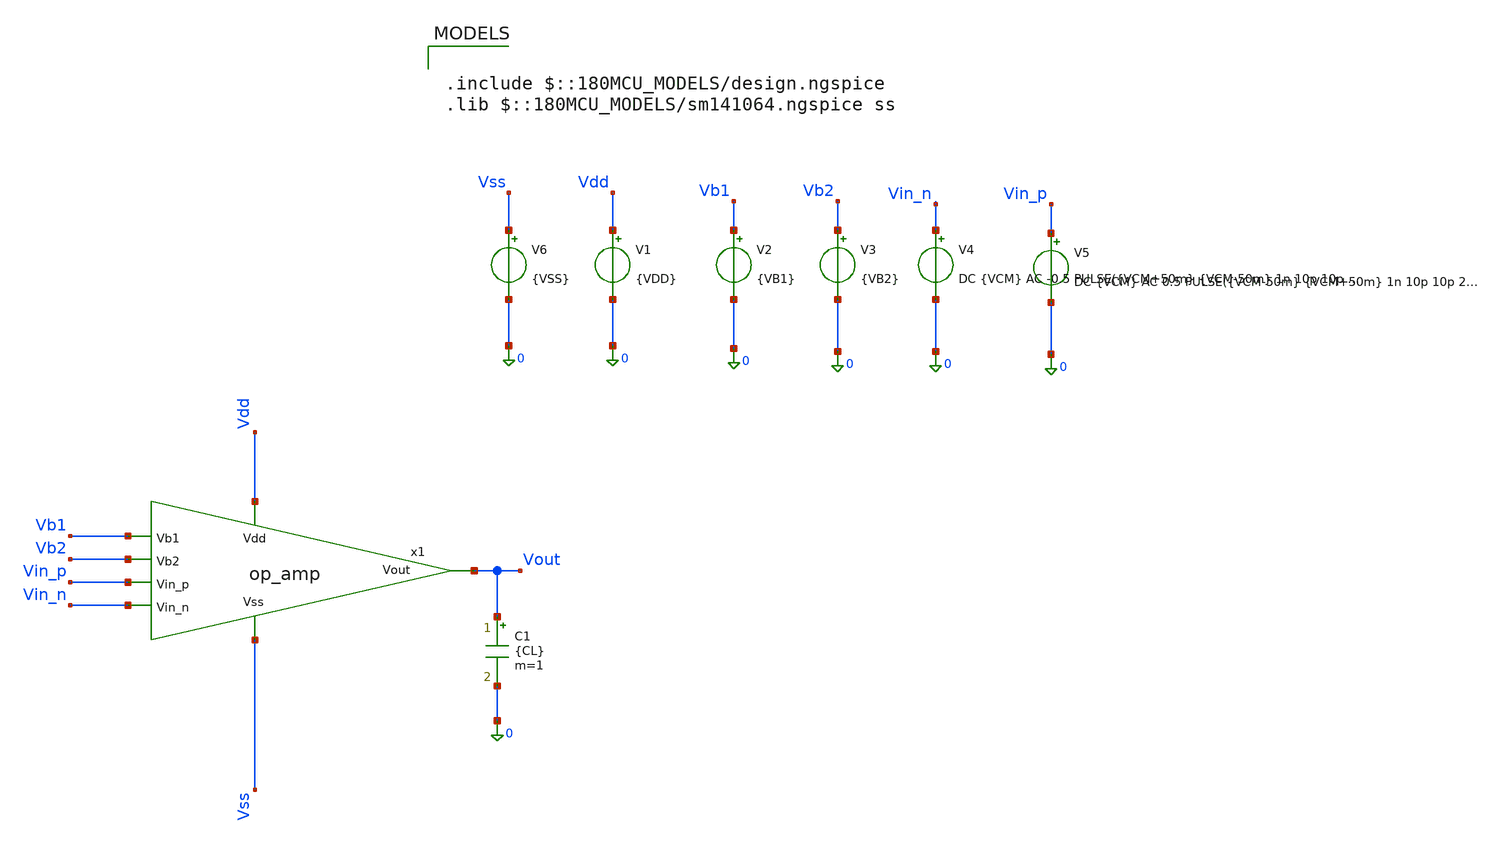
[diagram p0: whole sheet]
** sch_path: blocks/adc/lvds/ota_performance_test.sch
**.subckt ota_performance_test
x1 Vdd Vb1 Vout Vb2 Vin_p Vin_n Vss op_amp
V1 Vdd 0 {VDD}
V2 Vb1 0 {VB1}
V3 Vb2 0 {VB2}
V4 Vin_n 0 DC {VCM} AC -0.5 PULSE({VCM+50m} {VCM-50m} 1n 10p 10p 20n 50n)
V5 Vin_p 0 DC {VCM} AC 0.5 PULSE({VCM-50m} {VCM+50m} 1n 10p 10p 20n 50n)
V6 Vss 0 {VSS}
C1 Vout 0 {CL} m=1
**** begin user architecture code


.param VDD=3.3
.param VSS=0
.param VCM=1.2
.param VB1=0.0
.param VB2=1.65
.param CL=10f
.options temp=27

.control
save all
set filetype=ascii
set wr_singlescale
set wr_vecnames
shell rm /foss/designs/trans_testing/ota_testing/ota_ac.txt
shell rm /foss/designs/trans_testing/ota_testing/ota_tran.txt

op


* AC gain
ac dec 1000 1 500G
let vin_diff_ac = v(Vin_p)-v(Vin_n)
let gain = v(Vout)/vin_diff_ac
wrdata /foss/designs/trans_testing/ota_testing/ota_ac.txt frequency db(gain) real(gain) imag(gain)
plot v(Vout)

* Transient slew rate
tran 1p 100n
let vin_diff = v(Vin_p)-v(Vin_n)
let slew = deriv(v(Vout))
plot v(Vout)

wrdata /foss/designs/trans_testing/ota_testing/ota_tran.txt time v(Vin_p) v(Vin_n) vin_diff v(Vout)
+ slew

.endc



.include $::180MCU_MODELS/design.ngspice
.lib $::180MCU_MODELS/sm141064.ngspice ss

**** end user architecture code
**.ends

* expanding   symbol:  op_amp.sym # of pins=7
** sym_path: blocks/adc/lvds/op_amp.sym
** sch_path: blocks/adc/lvds/op_amp.sch
.subckt op_amp Vdd Vb1 Vout Vb2 Vin_p Vin_n Vss
*.ipin Vdd
*.ipin Vb2
*.ipin Vin_p
*.ipin Vin_n
*.ipin Vb1
*.opin Vout
*.ipin Vss
XM1 net2 net3 Vdd Vdd pfet_03v3 L=0.28u W=10.5u nf=1 ad='int((nf+1)/2) * W/nf * 0.18u' as='int((nf+2)/2) * W/nf * 0.18u'
+ pd='2*int((nf+1)/2) * (W/nf + 0.18u)' ps='2*int((nf+2)/2) * (W/nf + 0.18u)' nrd='0.18u / W' nrs='0.18u / W'
+ sa=0 sb=0 sd=0 m=1
XM2 net1 net4 Vdd Vdd pfet_03v3 L=0.28u W=10.5u nf=1 ad='int((nf+1)/2) * W/nf * 0.18u' as='int((nf+2)/2) * W/nf * 0.18u'
+ pd='2*int((nf+1)/2) * (W/nf + 0.18u)' ps='2*int((nf+2)/2) * (W/nf + 0.18u)' nrd='0.18u / W' nrs='0.18u / W'
+ sa=0 sb=0 sd=0 m=1
XM3 net3 Vb2 net2 Vdd pfet_03v3 L=0.28u W=10.5u nf=1 ad='int((nf+1)/2) * W/nf * 0.18u' as='int((nf+2)/2) * W/nf * 0.18u'
+ pd='2*int((nf+1)/2) * (W/nf + 0.18u)' ps='2*int((nf+2)/2) * (W/nf + 0.18u)' nrd='0.18u / W' nrs='0.18u / W'
+ sa=0 sb=0 sd=0 m=1
XM4 net4 Vb2 net1 Vdd pfet_03v3 L=0.28u W=10.5u nf=1 ad='int((nf+1)/2) * W/nf * 0.18u' as='int((nf+2)/2) * W/nf * 0.18u'
+ pd='2*int((nf+1)/2) * (W/nf + 0.18u)' ps='2*int((nf+2)/2) * (W/nf + 0.18u)' nrd='0.18u / W' nrs='0.18u / W'
+ sa=0 sb=0 sd=0 m=1
XM5 net4 Vin_p net5 Vss nfet_03v3 L=0.28u W=52.5u nf=15 ad='int((nf+1)/2) * W/nf * 0.18u' as='int((nf+2)/2) * W/nf * 0.18u'
+ pd='2*int((nf+1)/2) * (W/nf + 0.18u)' ps='2*int((nf+2)/2) * (W/nf + 0.18u)' nrd='0.18u / W' nrs='0.18u / W'
+ sa=0 sb=0 sd=0 m=1
XM6 net3 Vin_n net5 Vss nfet_03v3 L=0.28u W=52.5u nf=15 ad='int((nf+1)/2) * W/nf * 0.18u' as='int((nf+2)/2) * W/nf * 0.18u'
+ pd='2*int((nf+1)/2) * (W/nf + 0.18u)' ps='2*int((nf+2)/2) * (W/nf + 0.18u)' nrd='0.18u / W' nrs='0.18u / W'
+ sa=0 sb=0 sd=0 m=1
XM7 net6 net4 Vdd Vdd pfet_03v3 L=0.28u W=10.5u nf=1 ad='int((nf+1)/2) * W/nf * 0.18u' as='int((nf+2)/2) * W/nf * 0.18u'
+ pd='2*int((nf+1)/2) * (W/nf + 0.18u)' ps='2*int((nf+2)/2) * (W/nf + 0.18u)' nrd='0.18u / W' nrs='0.18u / W'
+ sa=0 sb=0 sd=0 m=1
XM9 net7 net3 Vdd Vdd pfet_03v3 L=0.28u W=10.5u nf=1 ad='int((nf+1)/2) * W/nf * 0.18u' as='int((nf+2)/2) * W/nf * 0.18u'
+ pd='2*int((nf+1)/2) * (W/nf + 0.18u)' ps='2*int((nf+2)/2) * (W/nf + 0.18u)' nrd='0.18u / W' nrs='0.18u / W'
+ sa=0 sb=0 sd=0 m=1
XM11 net8 Vb2 net10 Vss nfet_03v3 L=0.28u W=5.25u nf=1 ad='int((nf+1)/2) * W/nf * 0.18u' as='int((nf+2)/2) * W/nf * 0.18u'
+ pd='2*int((nf+1)/2) * (W/nf + 0.18u)' ps='2*int((nf+2)/2) * (W/nf + 0.18u)' nrd='0.18u / W' nrs='0.18u / W'
+ sa=0 sb=0 sd=0 m=1
XM12 Vout Vb2 net9 Vss nfet_03v3 L=0.28u W=5.25u nf=1 ad='int((nf+1)/2) * W/nf * 0.18u' as='int((nf+2)/2) * W/nf * 0.18u'
+ pd='2*int((nf+1)/2) * (W/nf + 0.18u)' ps='2*int((nf+2)/2) * (W/nf + 0.18u)' nrd='0.18u / W' nrs='0.18u / W'
+ sa=0 sb=0 sd=0 m=1
XM13 net10 net8 0 Vss nfet_03v3 L=0.28u W=5.25u nf=1 ad='int((nf+1)/2) * W/nf * 0.18u' as='int((nf+2)/2) * W/nf * 0.18u'
+ pd='2*int((nf+1)/2) * (W/nf + 0.18u)' ps='2*int((nf+2)/2) * (W/nf + 0.18u)' nrd='0.18u / W' nrs='0.18u / W'
+ sa=0 sb=0 sd=0 m=1
XM14 net9 net8 0 Vss nfet_03v3 L=0.28u W=5.25u nf=1 ad='int((nf+1)/2) * W/nf * 0.18u' as='int((nf+2)/2) * W/nf * 0.18u'
+ pd='2*int((nf+1)/2) * (W/nf + 0.18u)' ps='2*int((nf+2)/2) * (W/nf + 0.18u)' nrd='0.18u / W' nrs='0.18u / W'
+ sa=0 sb=0 sd=0 m=1
XM8 net8 Vb1 net6 Vdd pfet_03v3 L=0.28u W=10.5u nf=1 ad='int((nf+1)/2) * W/nf * 0.18u' as='int((nf+2)/2) * W/nf * 0.18u'
+ pd='2*int((nf+1)/2) * (W/nf + 0.18u)' ps='2*int((nf+2)/2) * (W/nf + 0.18u)' nrd='0.18u / W' nrs='0.18u / W'
+ sa=0 sb=0 sd=0 m=1
XM10 Vout Vb1 net7 Vdd pfet_03v3 L=0.28u W=10.5u nf=1 ad='int((nf+1)/2) * W/nf * 0.18u' as='int((nf+2)/2) * W/nf * 0.18u'
+ pd='2*int((nf+1)/2) * (W/nf + 0.18u)' ps='2*int((nf+2)/2) * (W/nf + 0.18u)' nrd='0.18u / W' nrs='0.18u / W'
+ sa=0 sb=0 sd=0 m=1
ibias net5 Vss 300u
.ends

.end
